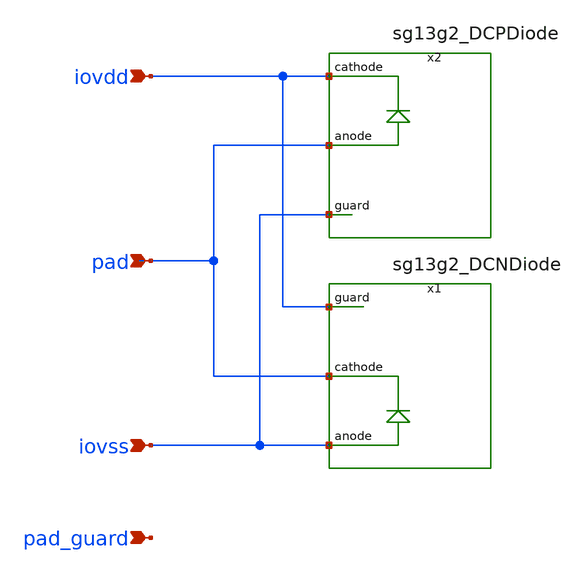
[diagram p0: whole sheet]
** sch_path: trident_test_structures/design_data/xschem/IOPadAnalog_submodules/DCP_DCN_diodes.sch
**.subckt DCP_DCN_diodes iovdd iovss pad pad_guard
*.ipin iovdd
*.ipin iovss
*.ipin pad
*.ipin pad_guard
x1 iovss pad iovdd sg13g2_DCNDiode
x2 pad iovdd iovss sg13g2_DCPDiode
**.ends
.end
